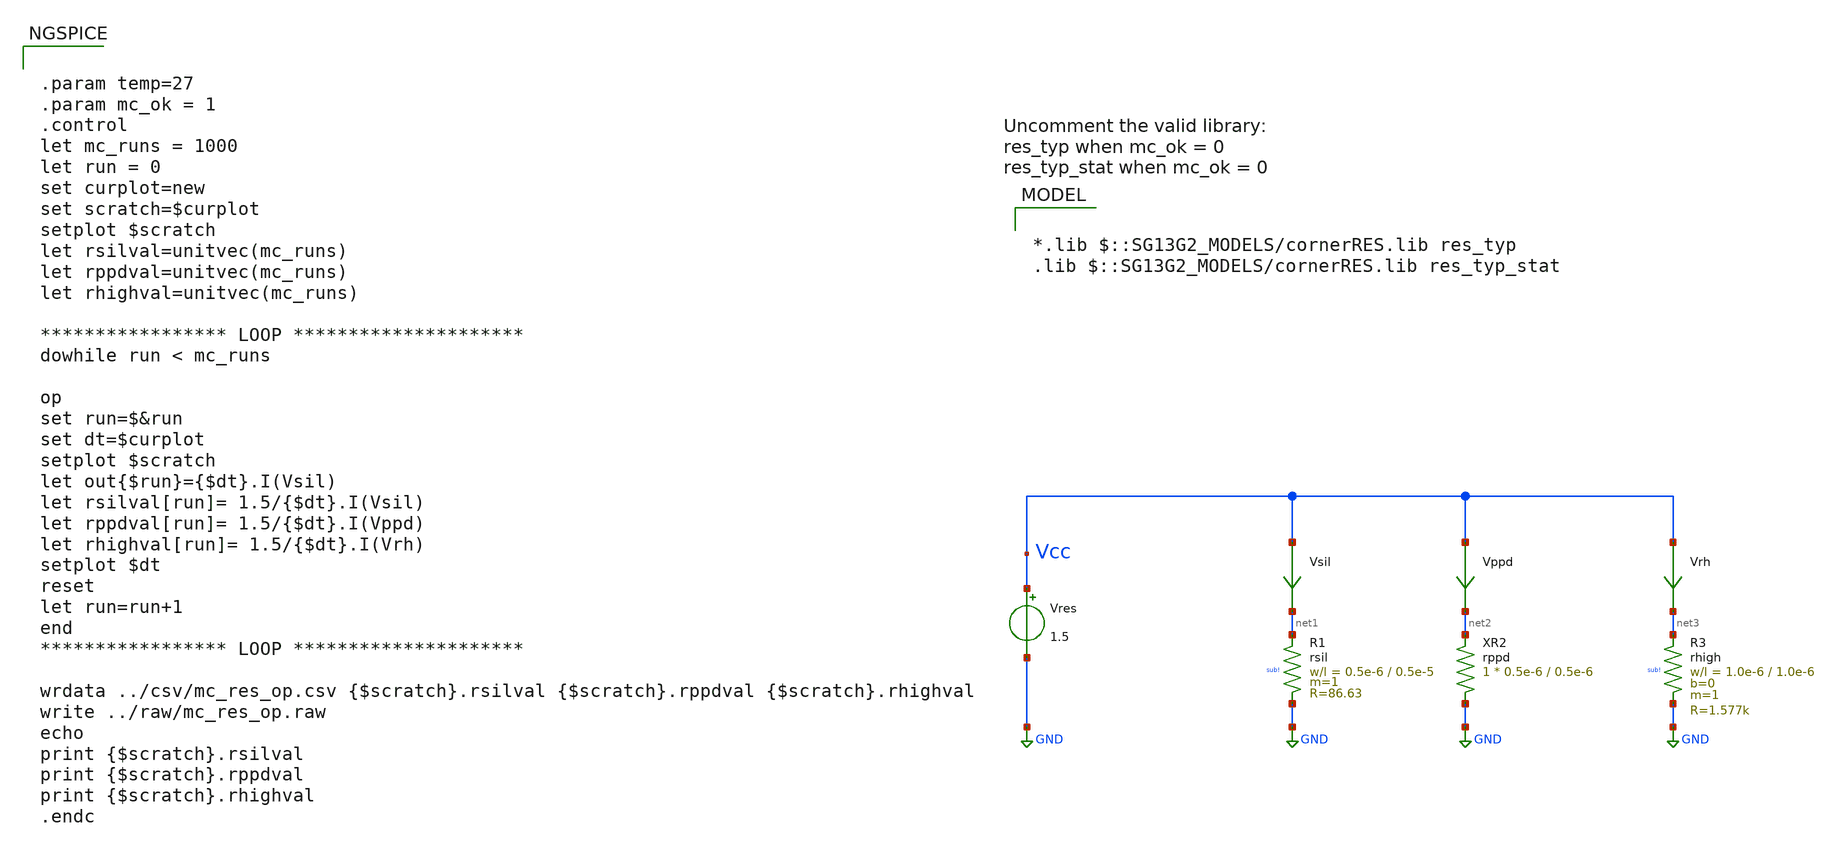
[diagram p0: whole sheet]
** sch_path: ihp-sg13g2/libs.tech/xschem/sg13g2_tests/mc_res_op.sch
* Copyright 2023 IHP PDK Authors
**.subckt mc_res_op
Vres Vcc GND 1.5
Vsil Vcc net1 0
.save i(vsil)
Vppd Vcc net2 0
.save i(vppd)
XR3 net3 GND sub! rhigh w=1.0e-6 l=1.0e-6 m=1 b=0 mm_ok=1
Vrh Vcc net3 0
.save i(vrh)
XR1 net1 GND sub! rsil w=0.5e-6 l=0.5e-5 m=1 mm_ok=1
XR2 GND net2 rppd w=0.5e-6 l=0.5e-6 m=1 R=7.0 Imax=0.3e-6
**** begin user architecture code

*.lib $::SG13G2_MODELS/cornerRES.lib res_typ
.lib $::SG13G2_MODELS/cornerRES.lib res_typ_stat



.param temp=27
.param mc_ok = 1
.control
let mc_runs = 1000
let run = 0
set curplot=new
set scratch=$curplot
setplot $scratch
let rsilval=unitvec(mc_runs)
let rppdval=unitvec(mc_runs)
let rhighval=unitvec(mc_runs)

***************** LOOP *********************
dowhile run < mc_runs

op
set run=$&run
set dt=$curplot
setplot $scratch
let out{$run}={$dt}.I(Vsil)
let rsilval[run]= 1.5/{$dt}.I(Vsil)
let rppdval[run]= 1.5/{$dt}.I(Vppd)
let rhighval[run]= 1.5/{$dt}.I(Vrh)
setplot $dt
reset
let run=run+1
end
***************** LOOP *********************

wrdata ../csv/mc_res_op.csv {$scratch}.rsilval {$scratch}.rppdval {$scratch}.rhighval
write ../raw/mc_res_op.raw
echo
print {$scratch}.rsilval
print {$scratch}.rppdval
print {$scratch}.rhighval
.endc


**** end user architecture code
**.ends
.GLOBAL GND
.end
